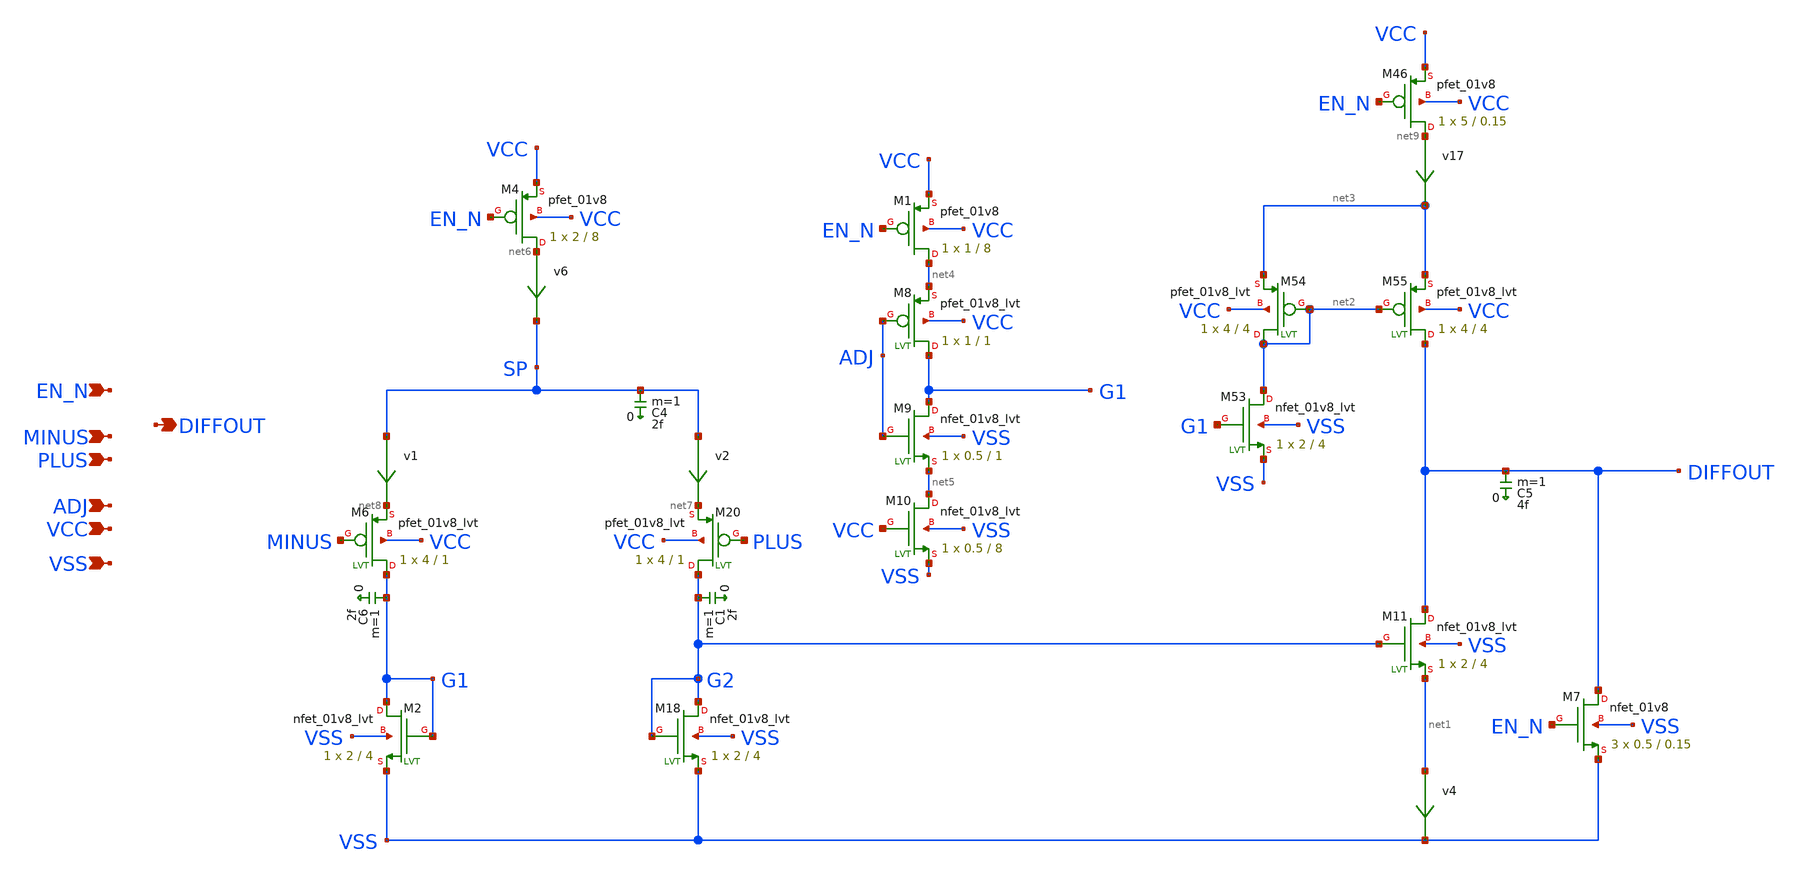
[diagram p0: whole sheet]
** sch_path: xyce/sky130A-xyce/libs.tech/xschem/sky130_tests/zero_opamp.sch
* Copyright 2020 Stefan Frederik Schippers
* Licensed under the Apache License, Version 2.0 (the "License");
* you may not use this file except in compliance with the License.
* You may obtain a copy of the License at
* https://www.apache.org/licenses/LICENSE-2.0
* Unless required by applicable law or agreed to in writing, software
* distributed under the License is distributed on an "AS IS" BASIS,
* WITHOUT WARRANTIES OR CONDITIONS OF ANY KIND, either express or implied.
* See the License for the specific language governing permissions and
* limitations under the License.
**.subckt zero_opamp PLUS MINUS EN_N VSS VCC DIFFOUT ADJ
*.ipin PLUS
*.ipin MINUS
*.ipin EN_N
*.ipin VSS
*.ipin VCC
*.opin DIFFOUT
*.ipin ADJ
C6 G1 0 2f m=1
XM4 net6 EN_N VCC VCC sky130_fd_pr__pfet_01v8 L=8 W=2 nf=1 ad='W * 0.29' as='W * 0.29' pd='W + 2 * 0.29'
+ ps='W + 2 * 0.29' nrd=0 nrs=0 sa=0 sb=0 sd=0 mult=1 m=1
XM18 G2 G2 VSS VSS sky130_fd_pr__nfet_01v8_lvt L=4 W=2 nf=1 ad='W * 0.29' as='W * 0.29' pd='2*(W + 0.29)'
+ ps='2*(W + 0.29)' nrd=0 nrs=0 sa=0 sb=0 sd=0 mult=1 m=1
XM2 G1 G1 VSS VSS sky130_fd_pr__nfet_01v8_lvt L=4 W=2 nf=1 ad='W * 0.29' as='W * 0.29' pd='2*(W + 0.29)'
+ ps='2*(W + 0.29)' nrd=0 nrs=0 sa=0 sb=0 sd=0 mult=1 m=1
XM20 G2 PLUS net7 VCC sky130_fd_pr__pfet_01v8_lvt L=1 W=4 nf=1 ad='W * 0.29' as='W * 0.29' pd='2*(W + 0.29)'
+ ps='2*(W + 0.29)' nrd=0 nrs=0 sa=0 sb=0 sd=0 mult=1 m=1
XM6 G1 MINUS net8 VCC sky130_fd_pr__pfet_01v8_lvt L=1 W=4 nf=1 ad='W * 0.29' as='W * 0.29' pd='2*(W + 0.29)'
+ ps='2*(W + 0.29)' nrd=0 nrs=0 sa=0 sb=0 sd=0 mult=1 m=1
v1 SP net8 0
.save i(v1)
C4 SP 0 2f m=1
C1 G2 0 2f m=1
C5 DIFFOUT 0 4f m=1
XM11 DIFFOUT G2 net1 VSS sky130_fd_pr__nfet_01v8_lvt L=4 W=2 nf=1 ad='W * 0.29' as='W * 0.29' pd='2*(W + 0.29)'
+ ps='2*(W + 0.29)' nrd=0 nrs=0 sa=0 sb=0 sd=0 mult=1 m=1
v2 SP net7 0
.save i(v2)
v4 net1 VSS 0
.save i(v4)
v6 net6 SP 0
.save i(v6)
XM7 DIFFOUT EN_N VSS VSS sky130_fd_pr__nfet_01v8 L=0.15 W=0.5 nf=1 ad='W * 0.29' as='W * 0.29' pd='2*(W + 0.29)'
+ ps='2*(W + 0.29)' nrd=0 nrs=0 sa=0 sb=0 sd=0 mult=3 m=3
XM46 net9 EN_N VCC VCC sky130_fd_pr__pfet_01v8 L=0.15 W=5 nf=1 ad='W * 0.29' as='W * 0.29' pd='W + 2 * 0.29'
+ ps='W + 2 * 0.29' nrd=0 nrs=0 sa=0 sb=0 sd=0 mult=1 m=1
v17 net9 net3 0
.save i(v17)
XM53 net2 G1 VSS VSS sky130_fd_pr__nfet_01v8_lvt L=4 W=2 nf=1 ad='W * 0.29' as='W * 0.29' pd='2*(W + 0.29)'
+ ps='2*(W + 0.29)' nrd=0 nrs=0 sa=0 sb=0 sd=0 mult=1 m=1
XM54 net2 net2 net3 VCC sky130_fd_pr__pfet_01v8_lvt L=4 W=4 nf=1 ad='W * 0.29' as='W * 0.29' pd='2*(W + 0.29)'
+ ps='2*(W + 0.29)' nrd=0 nrs=0 sa=0 sb=0 sd=0 mult=1 m=1
XM55 DIFFOUT net2 net3 VCC sky130_fd_pr__pfet_01v8_lvt L=4 W=4 nf=1 ad='W * 0.29' as='W * 0.29' pd='2*(W + 0.29)'
+ ps='2*(W + 0.29)' nrd=0 nrs=0 sa=0 sb=0 sd=0 mult=1 m=1
XM8 G1 ADJ net4 VCC sky130_fd_pr__pfet_01v8_lvt L=1 W=1 nf=1 ad='W * 0.29' as='W * 0.29' pd='W + 2 * 0.29'
+ ps='W + 2 * 0.29' nrd=0 nrs=0 sa=0 sb=0 sd=0 mult=1 m=1
XM9 G1 ADJ net5 VSS sky130_fd_pr__nfet_01v8_lvt L=1 W=0.5 nf=1 ad='W * 0.29' as='W * 0.29' pd='W + 2 * 0.29'
+ ps='W + 2 * 0.29' nrd=0 nrs=0 sa=0 sb=0 sd=0 mult=1 m=1
XM10 net5 VCC VSS VSS sky130_fd_pr__nfet_01v8_lvt L=8 W=0.5 nf=1 ad='W * 0.29' as='W * 0.29' pd='2*(W + 0.29)'
+ ps='2*(W + 0.29)' nrd=0 nrs=0 sa=0 sb=0 sd=0 mult=1 m=1
XM1 net4 EN_N VCC VCC sky130_fd_pr__pfet_01v8 L=8 W=1 nf=1 ad='W * 0.29' as='W * 0.29' pd='W + 2 * 0.29'
+ ps='W + 2 * 0.29' nrd=0 nrs=0 sa=0 sb=0 sd=0 mult=1 m=1
**** begin user architecture code

.include $::SKYWATER_MODELS/cells/nfet_01v8/sky130_fd_pr__nfet_01v8__tt.corner.spice
.include $::SKYWATER_MODELS/cells/nfet_01v8_lvt/sky130_fd_pr__nfet_01v8_lvt__tt.corner.spice
.include $::SKYWATER_MODELS/cells/pfet_01v8/sky130_fd_pr__pfet_01v8__tt.corner.spice
.include $::SKYWATER_MODELS/cells/nfet_03v3_nvt/sky130_fd_pr__nfet_03v3_nvt__tt.corner.spice
.include $::SKYWATER_MODELS/cells/nfet_05v0_nvt/sky130_fd_pr__nfet_05v0_nvt__tt.corner.spice
.include $::SKYWATER_MODELS/cells/esd_nfet_01v8/sky130_fd_pr__esd_nfet_01v8__tt.corner.spice
.include $::SKYWATER_MODELS/cells/pfet_01v8_lvt/sky130_fd_pr__pfet_01v8_lvt__tt.corner.spice
.include $::SKYWATER_MODELS/cells/pfet_01v8_hvt/sky130_fd_pr__pfet_01v8_hvt__tt.corner.spice
.include $::SKYWATER_MODELS/cells/esd_pfet_g5v0d10v5/sky130_fd_pr__esd_pfet_g5v0d10v5__tt.corner.spice
.include $::SKYWATER_MODELS/cells/pfet_g5v0d10v5/sky130_fd_pr__pfet_g5v0d10v5__tt.corner.spice
.include $::SKYWATER_MODELS/cells/pfet_g5v0d16v0/sky130_fd_pr__pfet_g5v0d16v0__tt.corner.spice
.include $::SKYWATER_MODELS/cells/nfet_g5v0d10v5/sky130_fd_pr__nfet_g5v0d10v5__tt.corner.spice
.include $::SKYWATER_MODELS/cells/nfet_g5v0d16v0/sky130_fd_pr__nfet_g5v0d16v0__tt_discrete.corner.spice
.include $::SKYWATER_MODELS/cells/esd_nfet_g5v0d10v5/sky130_fd_pr__esd_nfet_g5v0d10v5__tt.corner.spice
.include $::SKYWATER_MODELS/models/corners/tt/nonfet.spice
* Mismatch parameters
.include $::SKYWATER_MODELS/cells/nfet_01v8/sky130_fd_pr__nfet_01v8__mismatch.corner.spice
.include $::SKYWATER_MODELS/cells/pfet_01v8/sky130_fd_pr__pfet_01v8__mismatch.corner.spice
.include $::SKYWATER_MODELS/cells/nfet_01v8_lvt/sky130_fd_pr__nfet_01v8_lvt__mismatch.corner.spice
.include $::SKYWATER_MODELS/cells/pfet_01v8_lvt/sky130_fd_pr__pfet_01v8_lvt__mismatch.corner.spice
.include $::SKYWATER_MODELS/cells/pfet_01v8_hvt/sky130_fd_pr__pfet_01v8_hvt__mismatch.corner.spice
.include $::SKYWATER_MODELS/cells/nfet_g5v0d10v5/sky130_fd_pr__nfet_g5v0d10v5__mismatch.corner.spice
.include $::SKYWATER_MODELS/cells/pfet_g5v0d10v5/sky130_fd_pr__pfet_g5v0d10v5__mismatch.corner.spice
.include $::SKYWATER_MODELS/cells/nfet_05v0_nvt/sky130_fd_pr__nfet_05v0_nvt__mismatch.corner.spice
.include $::SKYWATER_MODELS/cells/nfet_03v3_nvt/sky130_fd_pr__nfet_03v3_nvt__mismatch.corner.spice
* Resistor$::SKYWATER_MODELS/Capacitor
.include $::SKYWATER_MODELS/models/r+c/res_typical__cap_typical.spice
.include $::SKYWATER_MODELS/models/r+c/res_typical__cap_typical__lin.spice
* Special cells
.include $::SKYWATER_MODELS/models/corners/tt/specialized_cells.spice
* All models
.include $::SKYWATER_MODELS/models/all.spice
* Corner
.include $::SKYWATER_MODELS/models/corners/tt/rf.spice

**** end user architecture code
**.ends
**** begin user architecture code

* .option SCALE=1e-6
.option method=gear seed=12

* this experimental option enables mos model bin
* selection based on W/NF instead of W
.option wnflag=1

.param VCC=1.8
* .param VCCGAUSS=agauss(1.8, 0.05, 1)
* .param VCC=VCCGAUSS
.param VDL=0.7
.param ABSVAR=0.02
.temp 25

** to generate following file:
** copy .../xschem_sky130/sky130_tests/stimuli.test_comparator to simulation directory
** then do 'Simulation->Utile Stimuli Editor (GUI)' and press 'Translate'
.include "stimuli_bandgap_opamp.cir"

** variation marameters:
* .param sky130_fd_pr__nfet_01v8_lvt__vth0_slope_spectre='agauss(0, ABSVAR, 3)/sky130_fd_pr__nfet_01v8_lvt__vth0_slope'
* .param sky130_fd_pr__pfet_01v8_lvt__vth0_slope_spectre='agauss(0, ABSVAR, 3)/sky130_fd_pr__pfet_01v8_lvt__vth0_slope'

* .tran 0.1n 900n uic

.control
  let run=1
  dowhile run <= 1
    if run > 1
      reset
      set appendwrite
    end
    save all
    * save saout cal i(vvcc) en plus minus
    tran 1n 10000n uic
    plot saout
    plot plus minus
    write bandgap_opamp.raw
    let run = run + 1
  end
.endc


**** end user architecture code
.end
